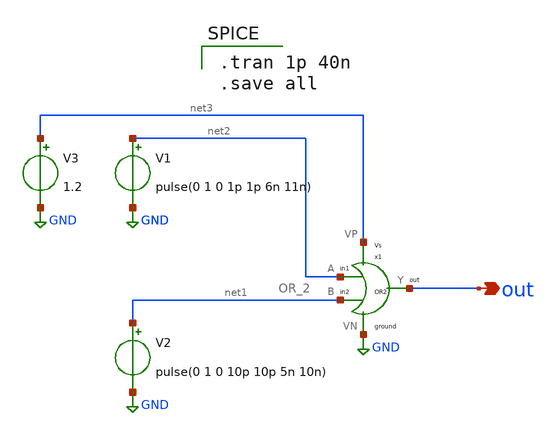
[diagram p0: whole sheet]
** sch_path: component/OR2/OR_test.sch
**.subckt OR_test out
*.opin out
x1 net1 net2 out net3 GND OR_2
V1 net2 GND pulse(0 1 0 1p 1p 6n 11n)
V2 net1 GND pulse(0 1 0 10p 10p 5n 10n)
V3 net3 GND 1.2
**** begin user architecture code

** opencircuitdesign pdks install
.lib $::SKYWATER_MODELS/sky130.lib.spice tt



.tran 1p 40n
.save all

**** end user architecture code
**.ends

* expanding   symbol:  Pico_project/OR2/OR_2.sym # of pins=5
** sym_path: component/OR2/OR_2.sym
** sch_path: component/OR2/OR_2.sch
.subckt OR_2 B A Y VP VN
*.iopin VP
*.iopin VN
*.ipin A
*.ipin B
*.opin Y
XM1 net1 B VN VN sky130_fd_pr__nfet_01v8 L=0.15 W=0.42 nf=1 ad='int((nf+1)/2) * W/nf * 0.29' as='int((nf+2)/2) * W/nf * 0.29'
+ pd='2*int((nf+1)/2) * (W/nf + 0.29)' ps='2*int((nf+2)/2) * (W/nf + 0.29)' nrd='0.29 / W' nrs='0.29 / W'
+ sa=0 sb=0 sd=0 mult=1 m=1
XM2 net1 A VN VN sky130_fd_pr__nfet_01v8 L=0.15 W=0.42 nf=1 ad='int((nf+1)/2) * W/nf * 0.29' as='int((nf+2)/2) * W/nf * 0.29'
+ pd='2*int((nf+1)/2) * (W/nf + 0.29)' ps='2*int((nf+2)/2) * (W/nf + 0.29)' nrd='0.29 / W' nrs='0.29 / W'
+ sa=0 sb=0 sd=0 mult=1 m=1
XM3 net1 B net2 VP sky130_fd_pr__pfet_01v8 L=0.15 W=2.52 nf=1 ad='int((nf+1)/2) * W/nf * 0.29' as='int((nf+2)/2) * W/nf * 0.29'
+ pd='2*int((nf+1)/2) * (W/nf + 0.29)' ps='2*int((nf+2)/2) * (W/nf + 0.29)' nrd='0.29 / W' nrs='0.29 / W'
+ sa=0 sb=0 sd=0 mult=1 m=1
XM4 net2 A VP VP sky130_fd_pr__pfet_01v8 L=0.15 W=2.52 nf=1 ad='int((nf+1)/2) * W/nf * 0.29' as='int((nf+2)/2) * W/nf * 0.29'
+ pd='2*int((nf+1)/2) * (W/nf + 0.29)' ps='2*int((nf+2)/2) * (W/nf + 0.29)' nrd='0.29 / W' nrs='0.29 / W'
+ sa=0 sb=0 sd=0 mult=1 m=1
x1 net1 Y VP VN INV
.ends


* expanding   symbol:  component/Inverter/INV.sym # of pins=4
** sym_path: component/Inverter/INV.sym
** sch_path: component/Inverter/INV.sch
.subckt INV X Y VP VN
*.ipin X
*.opin Y
*.iopin VN
*.iopin VP
XM8 Y X VP VP sky130_fd_pr__pfet_01v8 L=.18 W=1.512 nf=1 ad='int((nf+1)/2) * W/nf * 0.29' as='int((nf+2)/2) * W/nf * 0.29'
+ pd='2*int((nf+1)/2) * (W/nf + 0.29)' ps='2*int((nf+2)/2) * (W/nf + 0.29)' nrd='0.29 / W' nrs='0.29 / W'
+ sa=0 sb=0 sd=0 mult=1 m=1
XM4 Y X VN VN sky130_fd_pr__nfet_01v8 L=0.18 W=0.42 nf=1 ad='int((nf+1)/2) * W/nf * 0.29' as='int((nf+2)/2) * W/nf * 0.29'
+ pd='2*int((nf+1)/2) * (W/nf + 0.29)' ps='2*int((nf+2)/2) * (W/nf + 0.29)' nrd='0.29 / W' nrs='0.29 / W'
+ sa=0 sb=0 sd=0 mult=1 m=1
.ends

.GLOBAL GND
.end
